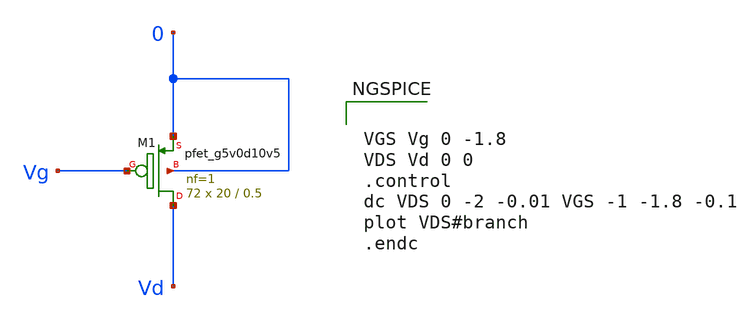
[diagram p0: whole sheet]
** sch_path: Analog_blocks/testing/test_pmos_current.sch
**.subckt test_pmos_current
XM1 Vd Vg 0 0 sky130_fd_pr__pfet_g5v0d10v5 L=0.5 W=20 nf=1 ad='int((nf+1)/2) * W/nf * 0.29' as='int((nf+2)/2) * W/nf * 0.29'
+ pd='2*int((nf+1)/2) * (W/nf + 0.29)' ps='2*int((nf+2)/2) * (W/nf + 0.29)' nrd='0.29 / W' nrs='0.29 / W'
+ sa=0 sb=0 sd=0 mult=72 m=72
**** begin user architecture code


.param mc_mm_switch=0
.param mc_pr_switch=0
.include ~/mabrains/Analog_blocks/models/sky130A/libs.ref/sky130_fd_pr/spice/sky130_fd_pr__nfet_01v8__tt.corner.spice
.include ~/mabrains/Analog_blocks/models/sky130A/libs.ref/sky130_fd_pr/spice/sky130_fd_pr__nfet_01v8_lvt__tt.corner.spice
.include ~/mabrains/Analog_blocks/models/sky130A/libs.ref/sky130_fd_pr/spice/sky130_fd_pr__pfet_01v8__tt.corner.spice
.include ~/mabrains/Analog_blocks/models/sky130A/libs.ref/sky130_fd_pr/spice/sky130_fd_pr__nfet_03v3_nvt__tt.corner.spice
.include ~/mabrains/Analog_blocks/models/sky130A/libs.ref/sky130_fd_pr/spice/sky130_fd_pr__nfet_05v0_nvt__tt.corner.spice
.include ~/mabrains/Analog_blocks/models/sky130A/libs.ref/sky130_fd_pr/spice/sky130_fd_pr__esd_nfet_01v8__tt.corner.spice
.include ~/mabrains/Analog_blocks/models/sky130A/libs.ref/sky130_fd_pr/spice/sky130_fd_pr__pfet_01v8_lvt__tt.corner.spice
.include ~/mabrains/Analog_blocks/models/sky130A/libs.ref/sky130_fd_pr/spice/sky130_fd_pr__pfet_01v8_hvt__tt.corner.spice
.include ~/mabrains/Analog_blocks/models/sky130A/libs.ref/sky130_fd_pr/spice/sky130_fd_pr__esd_pfet_g5v0d10v5__tt.corner.spice
.include ~/mabrains/Analog_blocks/models/sky130A/libs.ref/sky130_fd_pr/spice/sky130_fd_pr__pfet_g5v0d10v5__tt.corner.spice
.include ~/mabrains/Analog_blocks/models/sky130A/libs.ref/sky130_fd_pr/spice/sky130_fd_pr__pfet_g5v0d16v0__tt.corner.spice
.include ~/mabrains/Analog_blocks/models/sky130A/libs.ref/sky130_fd_pr/spice/sky130_fd_pr__nfet_g5v0d10v5__tt.corner.spice
.include ~/mabrains/Analog_blocks/models/sky130A/libs.ref/sky130_fd_pr/spice/sky130_fd_pr__nfet_g5v0d16v0__tt_discrete.corner.spice
.include ~/mabrains/Analog_blocks/models/sky130A/libs.ref/sky130_fd_pr/spice/sky130_fd_pr__esd_nfet_g5v0d10v5__tt.corner.spice
.include ~/mabrains/Analog_blocks/models/sky130A/libs.ref/sky130_fd_pr/spice/sky130_fd_pr__nfet_20v0__tt_discrete.corner.spice
.include ~/mabrains/Analog_blocks/models/sky130A/libs.ref/sky130_fd_pr/spice/sky130_fd_pr__pfet_20v0__tt_discrete.corner.spice
.include ~/mabrains/Analog_blocks/models/sky130A/libs.tech/ngspice/corners/tt/nonfet.spice
* Mismatch parameters
.include ~/mabrains/Analog_blocks/models/sky130A/libs.ref/sky130_fd_pr/spice/sky130_fd_pr__nfet_01v8__mismatch.corner.spice
.include ~/mabrains/Analog_blocks/models/sky130A/libs.ref/sky130_fd_pr/spice/sky130_fd_pr__pfet_01v8__mismatch.corner.spice
.include ~/mabrains/Analog_blocks/models/sky130A/libs.ref/sky130_fd_pr/spice/sky130_fd_pr__nfet_01v8_lvt__mismatch.corner.spice
.include ~/mabrains/Analog_blocks/models/sky130A/libs.ref/sky130_fd_pr/spice/sky130_fd_pr__pfet_01v8_lvt__mismatch.corner.spice
.include ~/mabrains/Analog_blocks/models/sky130A/libs.ref/sky130_fd_pr/spice/sky130_fd_pr__pfet_01v8_hvt__mismatch.corner.spice
.include ~/mabrains/Analog_blocks/models/sky130A/libs.ref/sky130_fd_pr/spice/sky130_fd_pr__nfet_g5v0d10v5__mismatch.corner.spice
.include ~/mabrains/Analog_blocks/models/sky130A/libs.ref/sky130_fd_pr/spice/sky130_fd_pr__pfet_g5v0d10v5__mismatch.corner.spice
.include ~/mabrains/Analog_blocks/models/sky130A/libs.ref/sky130_fd_pr/spice/sky130_fd_pr__nfet_05v0_nvt__mismatch.corner.spice
.include ~/mabrains/Analog_blocks/models/sky130A/libs.ref/sky130_fd_pr/spice/sky130_fd_pr__nfet_03v3_nvt__mismatch.corner.spice
* Resistor/Capacitor
.include ~/mabrains/Analog_blocks/models/sky130A/libs.tech/ngspice/r+c/res_typical__cap_typical.spice
.include ~/mabrains/Analog_blocks/models/sky130A/libs.tech/ngspice/r+c/res_typical__cap_typical__lin.spice
* Special cells
.include ~/mabrains/Analog_blocks/models/sky130A/libs.tech/ngspice/corners/tt/specialized_cells.spice
* All models
.include ~/mabrains/Analog_blocks/models/sky130A/libs.tech/ngspice/all.spice
* Corner
.include ~/mabrains/Analog_blocks/models/sky130A/libs.tech/ngspice/corners/tt/rf.spice





VGS Vg 0 -1.8
VDS Vd 0 0
.control
dc VDS 0 -2 -0.01 VGS -1 -1.8 -0.1
plot VDS#branch
.endc


**** end user architecture code
**.ends
.end
